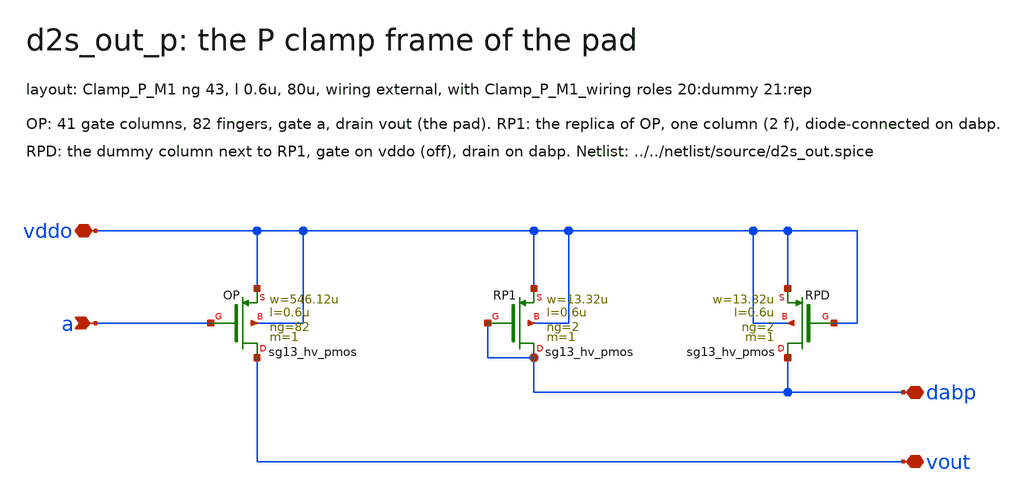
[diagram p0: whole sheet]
** sch_path: macros/sg13cmos5l_IOPadDiff2Single/schematic/xschem/d2s_out_p.sch
**.subckt d2s_out_p vddo a vout dabp
*.iopin vddo
*.ipin a
*.iopin vout
*.iopin dabp
XOP vout a vddo vddo sg13_hv_pmos w=546.12u l=0.6u ng=82 m=1 mm_ok=1
XRP1 dabp dabp vddo vddo sg13_hv_pmos w=13.32u l=0.6u ng=2 m=1 mm_ok=1
XRPD dabp vddo vddo vddo sg13_hv_pmos w=13.32u l=0.6u ng=2 m=1 mm_ok=1
**.ends
.end
